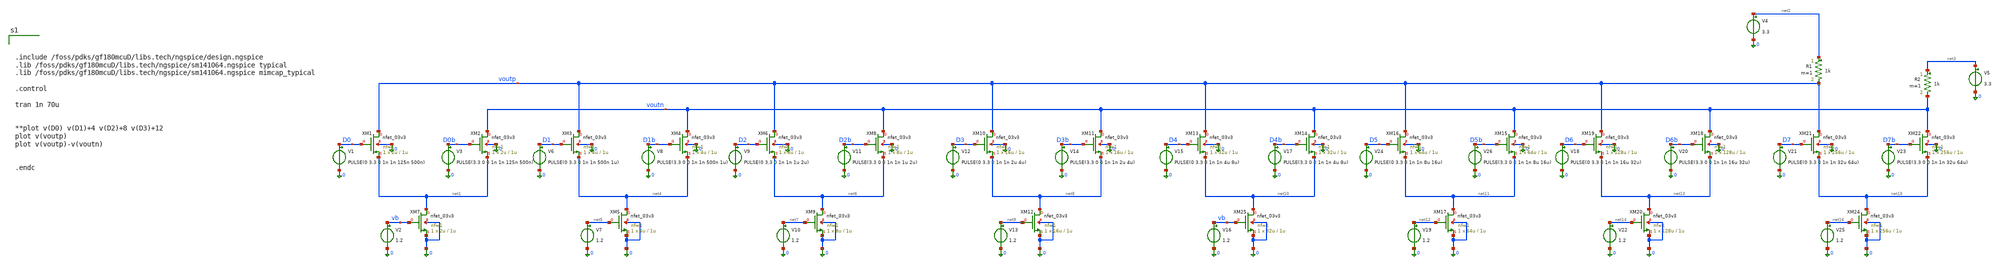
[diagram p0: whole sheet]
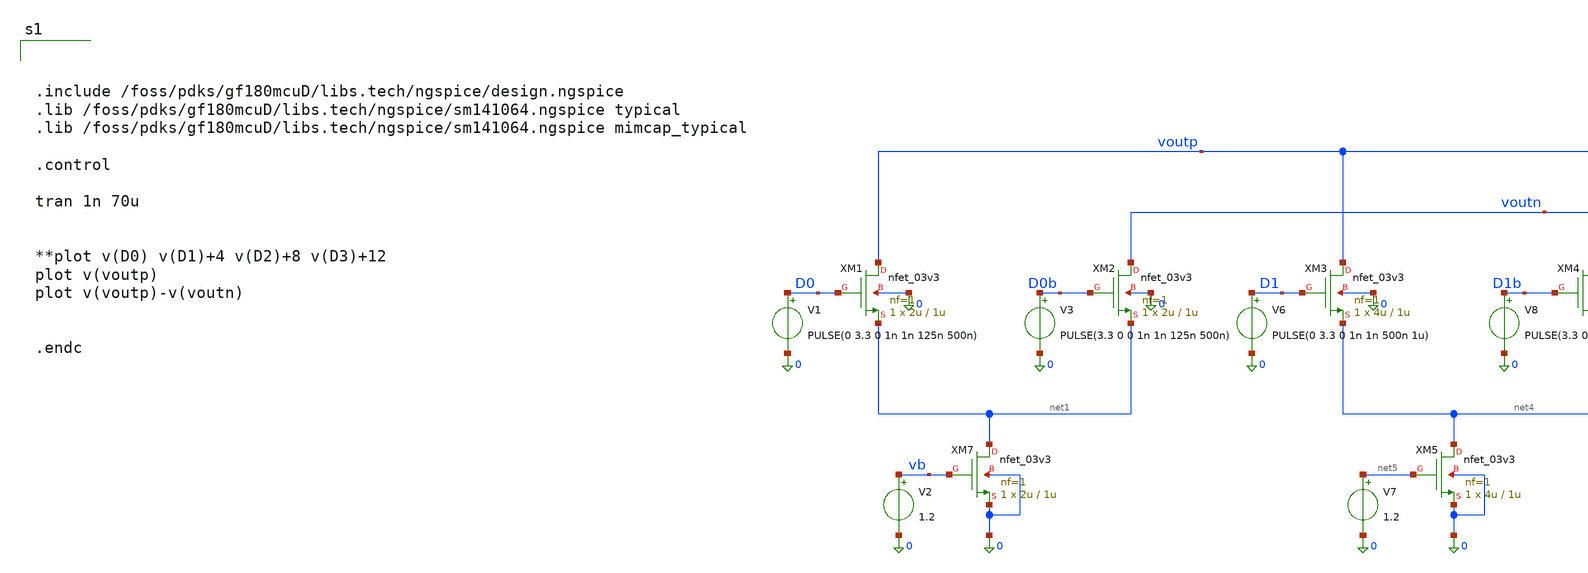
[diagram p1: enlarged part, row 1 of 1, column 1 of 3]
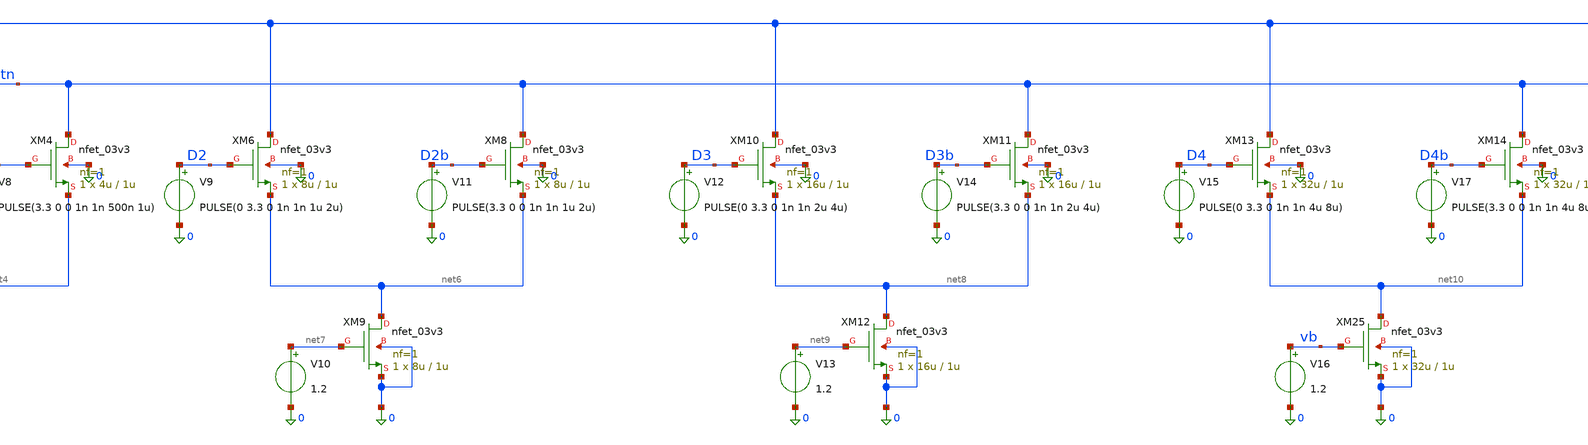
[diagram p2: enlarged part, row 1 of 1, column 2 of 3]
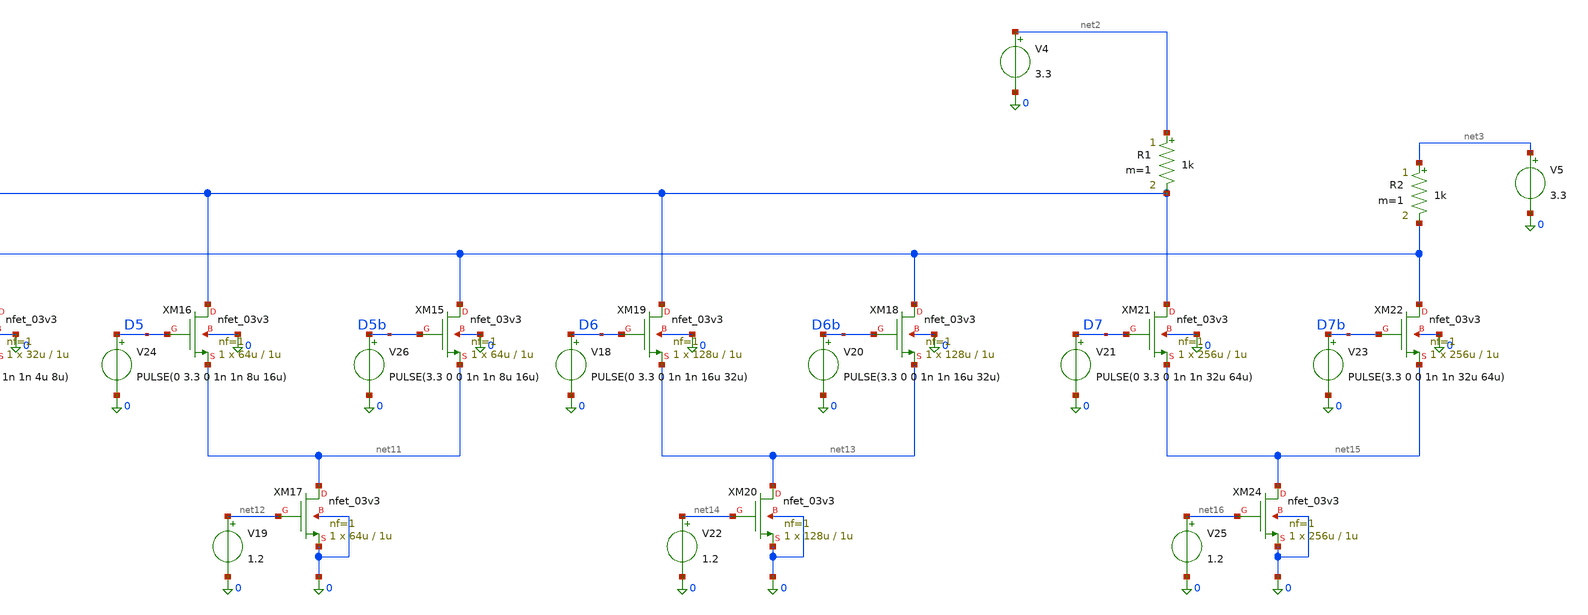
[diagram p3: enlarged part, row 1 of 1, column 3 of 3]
** sch_path: analog/dac/current_steering_dac.sch
**.subckt current_steering_dac
XM1 voutp D0 net1 0 nfet_03v3 L=1u W=2u nf=1 ad='int((nf+1)/2) * W/nf * 0.18u' as='int((nf+2)/2) * W/nf * 0.18u'
+ pd='2*int((nf+1)/2) * (W/nf + 0.18u)' ps='2*int((nf+2)/2) * (W/nf + 0.18u)' nrd='0.18u / W' nrs='0.18u / W'
+ sa=0 sb=0 sd=0 m=1
XM2 voutn D0b net1 0 nfet_03v3 L=1u W=2u nf=1 ad='int((nf+1)/2) * W/nf * 0.18u' as='int((nf+2)/2) * W/nf * 0.18u'
+ pd='2*int((nf+1)/2) * (W/nf + 0.18u)' ps='2*int((nf+2)/2) * (W/nf + 0.18u)' nrd='0.18u / W' nrs='0.18u / W'
+ sa=0 sb=0 sd=0 m=1
XM7 net1 vb 0 0 nfet_03v3 L=1u W=2u nf=1 ad='int((nf+1)/2) * W/nf * 0.18u' as='int((nf+2)/2) * W/nf * 0.18u'
+ pd='2*int((nf+1)/2) * (W/nf + 0.18u)' ps='2*int((nf+2)/2) * (W/nf + 0.18u)' nrd='0.18u / W' nrs='0.18u / W'
+ sa=0 sb=0 sd=0 m=1
V1 D0 0 PULSE(0 3.3 0 1n 1n 125n 500n)
V2 vb 0 1.2
V3 D0b 0 PULSE(3.3 0 0 1n 1n 125n 500n)
R1 net2 voutp 1k m=1
R2 net3 voutn 1k m=1
V4 net2 0 3.3
V5 net3 0 3.3
XM3 voutp D1 net4 0 nfet_03v3 L=1u W=4u nf=1 ad='int((nf+1)/2) * W/nf * 0.18u' as='int((nf+2)/2) * W/nf * 0.18u'
+ pd='2*int((nf+1)/2) * (W/nf + 0.18u)' ps='2*int((nf+2)/2) * (W/nf + 0.18u)' nrd='0.18u / W' nrs='0.18u / W'
+ sa=0 sb=0 sd=0 m=1
XM4 voutn D1b net4 0 nfet_03v3 L=1u W=4u nf=1 ad='int((nf+1)/2) * W/nf * 0.18u' as='int((nf+2)/2) * W/nf * 0.18u'
+ pd='2*int((nf+1)/2) * (W/nf + 0.18u)' ps='2*int((nf+2)/2) * (W/nf + 0.18u)' nrd='0.18u / W' nrs='0.18u / W'
+ sa=0 sb=0 sd=0 m=1
XM5 net4 net5 0 0 nfet_03v3 L=1u W=4u nf=1 ad='int((nf+1)/2) * W/nf * 0.18u' as='int((nf+2)/2) * W/nf * 0.18u'
+ pd='2*int((nf+1)/2) * (W/nf + 0.18u)' ps='2*int((nf+2)/2) * (W/nf + 0.18u)' nrd='0.18u / W' nrs='0.18u / W'
+ sa=0 sb=0 sd=0 m=1
V6 D1 0 PULSE(0 3.3 0 1n 1n 500n 1u)
V7 net5 0 1.2
V8 D1b 0 PULSE(3.3 0 0 1n 1n 500n 1u)
XM6 voutp D2 net6 0 nfet_03v3 L=1u W=8u nf=1 ad='int((nf+1)/2) * W/nf * 0.18u' as='int((nf+2)/2) * W/nf * 0.18u'
+ pd='2*int((nf+1)/2) * (W/nf + 0.18u)' ps='2*int((nf+2)/2) * (W/nf + 0.18u)' nrd='0.18u / W' nrs='0.18u / W'
+ sa=0 sb=0 sd=0 m=1
XM8 voutn D2b net6 0 nfet_03v3 L=1u W=8u nf=1 ad='int((nf+1)/2) * W/nf * 0.18u' as='int((nf+2)/2) * W/nf * 0.18u'
+ pd='2*int((nf+1)/2) * (W/nf + 0.18u)' ps='2*int((nf+2)/2) * (W/nf + 0.18u)' nrd='0.18u / W' nrs='0.18u / W'
+ sa=0 sb=0 sd=0 m=1
XM9 net6 net7 0 0 nfet_03v3 L=1u W=8u nf=1 ad='int((nf+1)/2) * W/nf * 0.18u' as='int((nf+2)/2) * W/nf * 0.18u'
+ pd='2*int((nf+1)/2) * (W/nf + 0.18u)' ps='2*int((nf+2)/2) * (W/nf + 0.18u)' nrd='0.18u / W' nrs='0.18u / W'
+ sa=0 sb=0 sd=0 m=1
V9 D2 0 PULSE(0 3.3 0 1n 1n 1u 2u)
V10 net7 0 1.2
V11 D2b 0 PULSE(3.3 0 0 1n 1n 1u 2u)
XM10 voutp D3 net8 0 nfet_03v3 L=1u W=16u nf=1 ad='int((nf+1)/2) * W/nf * 0.18u' as='int((nf+2)/2) * W/nf * 0.18u'
+ pd='2*int((nf+1)/2) * (W/nf + 0.18u)' ps='2*int((nf+2)/2) * (W/nf + 0.18u)' nrd='0.18u / W' nrs='0.18u / W'
+ sa=0 sb=0 sd=0 m=1
XM11 voutn D3b net8 0 nfet_03v3 L=1u W=16u nf=1 ad='int((nf+1)/2) * W/nf * 0.18u' as='int((nf+2)/2) * W/nf * 0.18u'
+ pd='2*int((nf+1)/2) * (W/nf + 0.18u)' ps='2*int((nf+2)/2) * (W/nf + 0.18u)' nrd='0.18u / W' nrs='0.18u / W'
+ sa=0 sb=0 sd=0 m=1
XM12 net8 net9 0 0 nfet_03v3 L=1u W=16u nf=1 ad='int((nf+1)/2) * W/nf * 0.18u' as='int((nf+2)/2) * W/nf * 0.18u'
+ pd='2*int((nf+1)/2) * (W/nf + 0.18u)' ps='2*int((nf+2)/2) * (W/nf + 0.18u)' nrd='0.18u / W' nrs='0.18u / W'
+ sa=0 sb=0 sd=0 m=1
V12 D3 0 PULSE(0 3.3 0 1n 1n 2u 4u)
V13 net9 0 1.2
V14 D3b 0 PULSE(3.3 0 0 1n 1n 2u 4u)
XM13 voutp D4 net10 0 nfet_03v3 L=1u W=32u nf=1 ad='int((nf+1)/2) * W/nf * 0.18u' as='int((nf+2)/2) * W/nf * 0.18u'
+ pd='2*int((nf+1)/2) * (W/nf + 0.18u)' ps='2*int((nf+2)/2) * (W/nf + 0.18u)' nrd='0.18u / W' nrs='0.18u / W'
+ sa=0 sb=0 sd=0 m=1
V15 D4 0 PULSE(0 3.3 0 1n 1n 4u 8u)
V16 vb 0 1.2
V17 D4b 0 PULSE(3.3 0 0 1n 1n 4u 8u)
XM16 voutp D5 net11 0 nfet_03v3 L=1u W=64u nf=1 ad='int((nf+1)/2) * W/nf * 0.18u' as='int((nf+2)/2) * W/nf * 0.18u'
+ pd='2*int((nf+1)/2) * (W/nf + 0.18u)' ps='2*int((nf+2)/2) * (W/nf + 0.18u)' nrd='0.18u / W' nrs='0.18u / W'
+ sa=0 sb=0 sd=0 m=1
V18 D6 0 PULSE(0 3.3 0 1n 1n 16u 32u)
V19 net12 0 1.2
V20 D6b 0 PULSE(3.3 0 0 1n 1n 16u 32u)
XM19 voutp D6 net13 0 nfet_03v3 L=1u W=128u nf=1 ad='int((nf+1)/2) * W/nf * 0.18u' as='int((nf+2)/2) * W/nf * 0.18u'
+ pd='2*int((nf+1)/2) * (W/nf + 0.18u)' ps='2*int((nf+2)/2) * (W/nf + 0.18u)' nrd='0.18u / W' nrs='0.18u / W'
+ sa=0 sb=0 sd=0 m=1
V21 D7 0 PULSE(0 3.3 0 1n 1n 32u 64u)
V22 net14 0 1.2
V23 D7b 0 PULSE(3.3 0 0 1n 1n 32u 64u)
XM24 net15 net16 0 0 nfet_03v3 L=1u W=256u nf=1 ad='int((nf+1)/2) * W/nf * 0.18u' as='int((nf+2)/2) * W/nf * 0.18u'
+ pd='2*int((nf+1)/2) * (W/nf + 0.18u)' ps='2*int((nf+2)/2) * (W/nf + 0.18u)' nrd='0.18u / W' nrs='0.18u / W'
+ sa=0 sb=0 sd=0 m=1
V25 net16 0 1.2
V24 D5 0 PULSE(0 3.3 0 1n 1n 8u 16u)
V26 D5b 0 PULSE(3.3 0 0 1n 1n 8u 16u)
XM14 voutn D4b net10 0 nfet_03v3 L=1u W=32u nf=1 ad='int((nf+1)/2) * W/nf * 0.18u' as='int((nf+2)/2) * W/nf * 0.18u'
+ pd='2*int((nf+1)/2) * (W/nf + 0.18u)' ps='2*int((nf+2)/2) * (W/nf + 0.18u)' nrd='0.18u / W' nrs='0.18u / W'
+ sa=0 sb=0 sd=0 m=1
XM25 net10 vb 0 0 nfet_03v3 L=1u W=32u nf=1 ad='int((nf+1)/2) * W/nf * 0.18u' as='int((nf+2)/2) * W/nf * 0.18u'
+ pd='2*int((nf+1)/2) * (W/nf + 0.18u)' ps='2*int((nf+2)/2) * (W/nf + 0.18u)' nrd='0.18u / W' nrs='0.18u / W'
+ sa=0 sb=0 sd=0 m=1
XM15 voutn D5b net11 0 nfet_03v3 L=1u W=64u nf=1 ad='int((nf+1)/2) * W/nf * 0.18u' as='int((nf+2)/2) * W/nf * 0.18u'
+ pd='2*int((nf+1)/2) * (W/nf + 0.18u)' ps='2*int((nf+2)/2) * (W/nf + 0.18u)' nrd='0.18u / W' nrs='0.18u / W'
+ sa=0 sb=0 sd=0 m=1
XM17 net11 net12 0 0 nfet_03v3 L=1u W=64u nf=1 ad='int((nf+1)/2) * W/nf * 0.18u' as='int((nf+2)/2) * W/nf * 0.18u'
+ pd='2*int((nf+1)/2) * (W/nf + 0.18u)' ps='2*int((nf+2)/2) * (W/nf + 0.18u)' nrd='0.18u / W' nrs='0.18u / W'
+ sa=0 sb=0 sd=0 m=1
XM18 voutn D6b net13 0 nfet_03v3 L=1u W=128u nf=1 ad='int((nf+1)/2) * W/nf * 0.18u' as='int((nf+2)/2) * W/nf * 0.18u'
+ pd='2*int((nf+1)/2) * (W/nf + 0.18u)' ps='2*int((nf+2)/2) * (W/nf + 0.18u)' nrd='0.18u / W' nrs='0.18u / W'
+ sa=0 sb=0 sd=0 m=1
XM20 net13 net14 0 0 nfet_03v3 L=1u W=128u nf=1 ad='int((nf+1)/2) * W/nf * 0.18u' as='int((nf+2)/2) * W/nf * 0.18u'
+ pd='2*int((nf+1)/2) * (W/nf + 0.18u)' ps='2*int((nf+2)/2) * (W/nf + 0.18u)' nrd='0.18u / W' nrs='0.18u / W'
+ sa=0 sb=0 sd=0 m=1
XM21 voutp D7 net15 0 nfet_03v3 L=1u W=256u nf=1 ad='int((nf+1)/2) * W/nf * 0.18u' as='int((nf+2)/2) * W/nf * 0.18u'
+ pd='2*int((nf+1)/2) * (W/nf + 0.18u)' ps='2*int((nf+2)/2) * (W/nf + 0.18u)' nrd='0.18u / W' nrs='0.18u / W'
+ sa=0 sb=0 sd=0 m=1
XM22 voutn D7b net15 0 nfet_03v3 L=1u W=256u nf=1 ad='int((nf+1)/2) * W/nf * 0.18u' as='int((nf+2)/2) * W/nf * 0.18u'
+ pd='2*int((nf+1)/2) * (W/nf + 0.18u)' ps='2*int((nf+2)/2) * (W/nf + 0.18u)' nrd='0.18u / W' nrs='0.18u / W'
+ sa=0 sb=0 sd=0 m=1
**** begin user architecture code



.include /foss/pdks/gf180mcuD/libs.tech/ngspice/design.ngspice
.lib /foss/pdks/gf180mcuD/libs.tech/ngspice/sm141064.ngspice typical
.lib /foss/pdks/gf180mcuD/libs.tech/ngspice/sm141064.ngspice mimcap_typical

.control

tran 1n 70u


**plot v(D0) v(D1)+4 v(D2)+8 v(D3)+12
plot v(voutp)
plot v(voutp)-v(voutn)


.endc



**** end user architecture code
**.ends
.end
